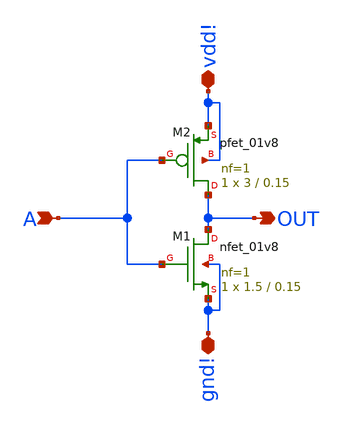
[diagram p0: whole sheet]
** sch_path: skywater_stuff/INV_VDD_GND.sch
**.subckt INV_VDD_GND A OUT vdd! gnd!
*.ipin A
*.opin OUT
*.iopin vdd!
*.iopin gnd!
XM2 OUT A vdd! vdd! sky130_fd_pr__pfet_01v8 L=0.15 W=3 nf=1 ad='int((nf+1)/2) * W/nf * 0.29' as='int((nf+2)/2) * W/nf * 0.29'
+ pd='2*int((nf+1)/2) * (W/nf + 0.29)' ps='2*int((nf+2)/2) * (W/nf + 0.29)' nrd='0.29 / W' nrs='0.29 / W'
+ sa=0 sb=0 sd=0 mult=1 m=1
XM1 OUT A gnd! gnd! sky130_fd_pr__nfet_01v8 L=0.15 W=1.5 nf=1 ad='int((nf+1)/2) * W/nf * 0.29' as='int((nf+2)/2) * W/nf * 0.29'
+ pd='2*int((nf+1)/2) * (W/nf + 0.29)' ps='2*int((nf+2)/2) * (W/nf + 0.29)' nrd='0.29 / W' nrs='0.29 / W'
+ sa=0 sb=0 sd=0 mult=1 m=1
**.ends
.end
